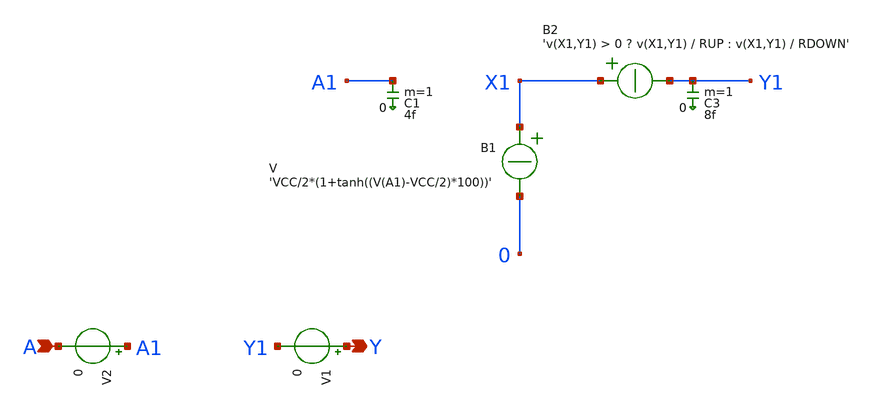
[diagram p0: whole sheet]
** sch_path: xschem_library_oa/ngspice/buf_ngspice/schematic/buf_ngspice.sch
* Copyright (C) 1998-2024 Stefan Frederik Schippers
* This program is free software; you can redistribute it and/or modify
* it under the terms of the GNU General Public License as published by
* the Free Software Foundation; either version 2 of the License, or
* (at your option) any later version.
* This program is distributed in the hope that it will be useful,
* but WITHOUT ANY WARRANTY; without even the implied warranty of
* MERCHANTABILITY or FITNESS FOR A PARTICULAR PURPOSE.  See the
* GNU General Public License for more details.
* You should have received a copy of the GNU General Public License
* along with this program; if not, write to the Free Software
**.subckt buf_ngspice A Y
*.ipin A
*.opin Y
B1 X1 0 V = 'VCC/2*(1+tanh((V(A1)-VCC/2)*100))'
C3 Y1 0 8f m=1
C1 A1 0 4f m=1
V1 Y Y1 0
V2 A1 A 0
B2 X1 Y1 I = 'v(X1,Y1) > 0 ? v(X1,Y1) / RUP : v(X1,Y1) / RDOWN'
**.ends
.end
